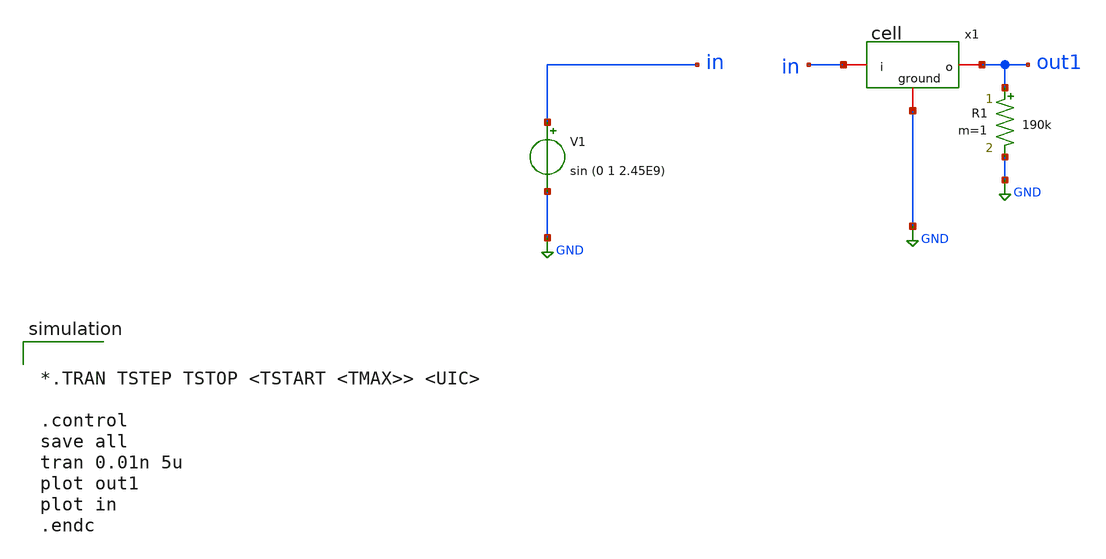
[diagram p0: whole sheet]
** sch_path: xschem/multiplier-full-1.sch
**.subckt multiplier-full-1
V1 in GND sin (0 1 2.45E9)
x1 out1 in GND cell
R1 out1 GND 190k m=1
**** begin user architecture code


*.TRAN TSTEP TSTOP <TSTART <TMAX>> <UIC>

.control
save all
tran 0.01n 5u
plot out1
plot in
.endc



** opencircuitdesign pdks install
.lib $::SKYWATER_MODELS/sky130.lib.spice tt


**** end user architecture code
**.ends

* expanding   symbol:  cell.sym # of pins=3
** sym_path: xschem/cell.sym
** sch_path: xschem/cell.sch
.subckt cell o i ground
*.iopin ground
*.iopin o
*.iopin i
XM10 net1 net1 ground net1 sky130_fd_pr__pfet_01v8_lvt L=0.35 W=40 nf=5 ad='int((5 + 1)/2) * 40 / 5 * 0.29'
+ as='int((5 + 2)/2) * 40 / 5 * 0.29' pd='2*int((5 + 1)/2) * (40 / 5 + 0.29)' ps='2*int((5 + 2)/2) * (40 / 5 + 0.29)'
+ nrd='0.29 / 40 ' nrs='0.29 / 40 ' sa=0 sb=0 sd=0 mult=1 m=1
XM1 o o net1 o sky130_fd_pr__pfet_01v8_lvt L=0.35 W=40 nf=5 ad='int((5 + 1)/2) * 40 / 5 * 0.29' as='int((5 + 2)/2) * 40 / 5 * 0.29'
+ pd='2*int((5 + 1)/2) * (40 / 5 + 0.29)' ps='2*int((5 + 2)/2) * (40 / 5 + 0.29)' nrd='0.29 / 40 ' nrs='0.29 / 40 '
+ sa=0 sb=0 sd=0 mult=1 m=1
XC3 o ground sky130_fd_pr__cap_mim_m3_1 W=30 L=30 MF=3 m=3
XC2 net1 i sky130_fd_pr__cap_mim_m3_1 W=30 L=30 MF=1 m=1
.ends

.GLOBAL GND
.end
